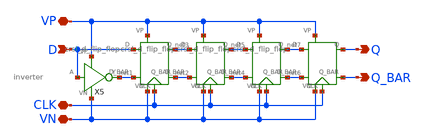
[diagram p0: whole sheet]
** sch_path: shift_register/schematics/4_bit_shift_register.sch
**.subckt 4_bit_shift_register VP VN Q Q_BAR D CLK
*.iopin VP
*.iopin VN
*.opin Q
*.opin Q_BAR
*.ipin D
*.iopin CLK
X1 D net1 net2 VP net3 CLK VN crsl_d_flip_flop
X2 net3 net2 net4 VP net5 CLK VN crsl_d_flip_flop
X3 net5 net4 net6 VP net7 CLK VN crsl_d_flip_flop
X4 net7 net6 Q_BAR VP Q CLK VN crsl_d_flip_flop
X5 D VP VN net1 inverter
**.ends
.end
